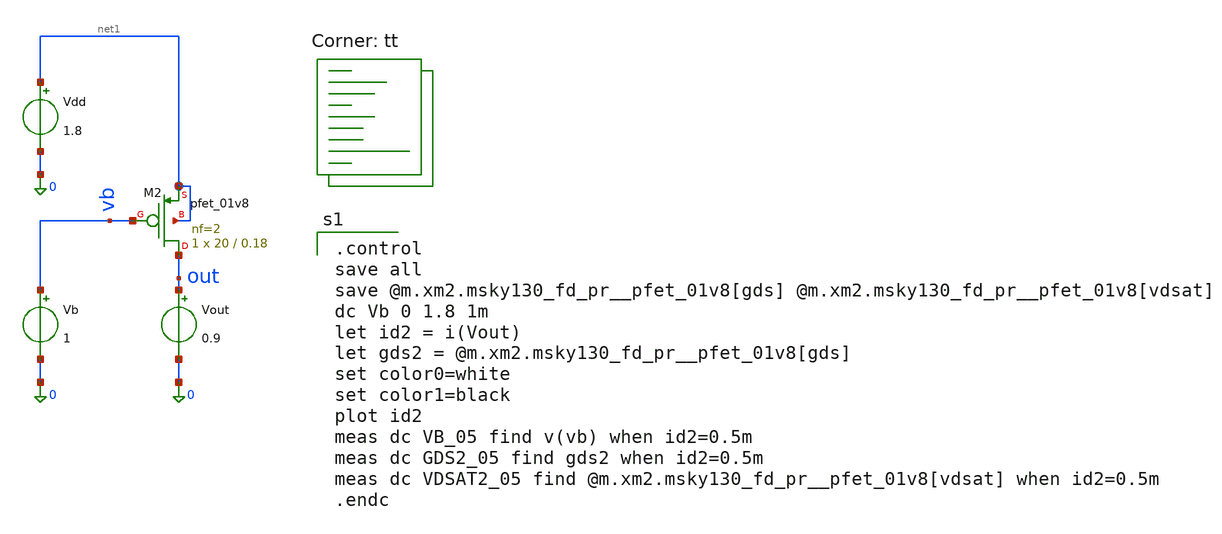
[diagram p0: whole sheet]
** sch_path: Homework 6 - Simulation on Open Source Softwares/Simulations/ex5_pmos.sch
**.subckt ex5_pmos
XM2 out vb net1 net1 sky130_fd_pr__pfet_01v8 L=0.18 W=20 nf=2 ad='int((2 + 1)/2) * 20 / 2 * 0.29' as='int((2 + 2)/2) * 20 / 2 * 0.29'
+ pd='2*int((2 + 1)/2) * (20 / 2 + 0.29)' ps='2*int((2 + 2)/2) * (20 / 2 + 0.29)' nrd='0.29 / 20 ' nrs='0.29 / 20 '
+ sa=0 sb=0 sd=0 mult=1 m=1
Vdd net1 0 1.8
Vb vb 0 1
Vout out 0 0.9
**** begin user architecture code
.lib $::SKYWATER_MODELS/sky130.lib.spice tt

.control
save all
save @m.xm2.msky130_fd_pr__pfet_01v8[gds] @m.xm2.msky130_fd_pr__pfet_01v8[vdsat]
dc Vb 0 1.8 1m
let id2 = i(Vout)
let gds2 = @m.xm2.msky130_fd_pr__pfet_01v8[gds]
set color0=white
set color1=black
plot id2
meas dc VB_05 find v(vb) when id2=0.5m
meas dc GDS2_05 find gds2 when id2=0.5m
meas dc VDSAT2_05 find @m.xm2.msky130_fd_pr__pfet_01v8[vdsat] when id2=0.5m
.endc

**** end user architecture code
**.ends
.end
